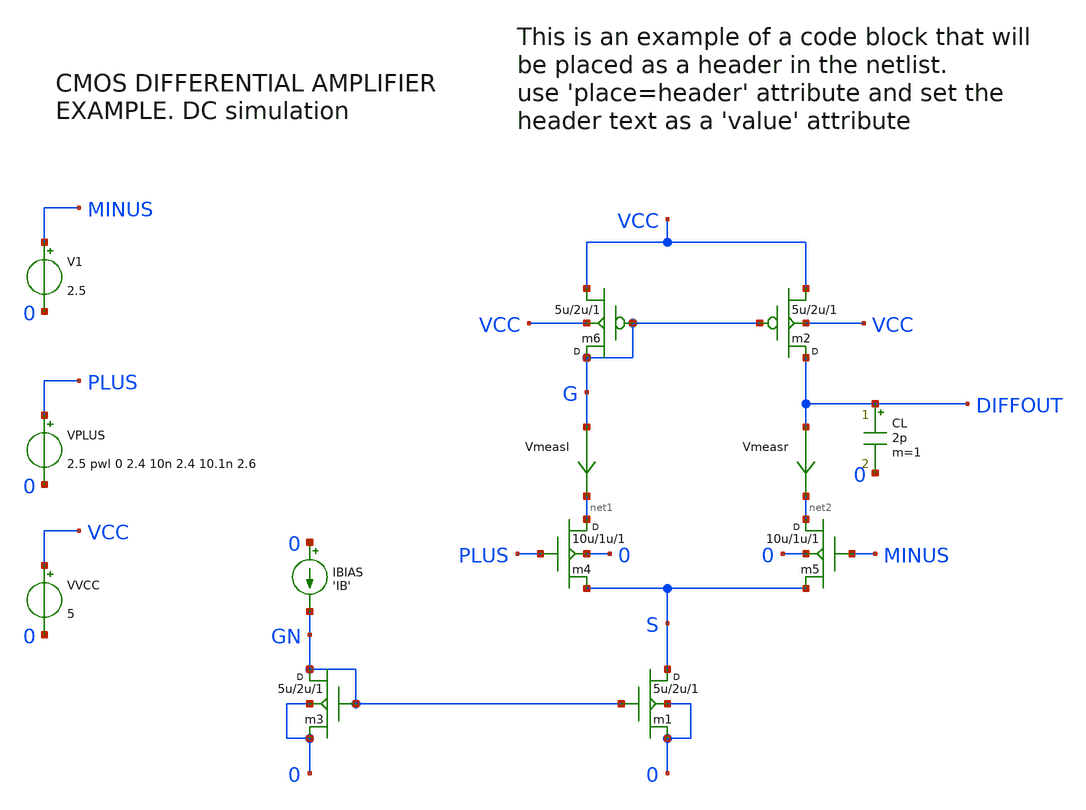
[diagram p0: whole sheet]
** sch_path: xschem_library/examples/cmos_example.sch
* Copyright (C) 1998-2023 Stefan Frederik Schippers
* This program is free software; you can redistribute it and/or modify
* it under the terms of the GNU General Public License as published by
* the Free Software Foundation; either version 2 of the License, or
* (at your option) any later version.
* This program is distributed in the hope that it will be useful,
* but WITHOUT ANY WARRANTY; without even the implied warranty of
* MERCHANTABILITY or FITNESS FOR A PARTICULAR PURPOSE.  See the
* GNU General Public License for more details.
* You should have received a copy of the GNU General Public License
* along with this program; if not, write to the Free Software

** ======================== **
** This is a netlist header **
** ======================== **

**.subckt cmos_example
m1 S GN 0 0 cmosn w=5u l=2u m=1
m2 DIFFOUT G VCC VCC cmosp w=5u l=2u m=1
VVCC VCC 0 5
m3 GN GN 0 0 cmosn w=5u l=2u m=1
IBIAS 0 GN 'IB'
m4 net1 PLUS S 0 cmosn w=10u l=1u m=1
m5 net2 MINUS S 0 cmosn w=10u l=1u m=1
m6 G G VCC VCC cmosp w=5u l=2u m=1
VPLUS PLUS 0 2.5 pwl 0 2.4 10n 2.4 10.1n 2.6
V1 MINUS 0 2.5
CL DIFFOUT 0 2p m=1
Vmeasr DIFFOUT net2 0
.save i(vmeasr)
Vmeasl G net1 0
.save i(vmeasl)
**** begin user architecture code


.temp 30
.param IB=1u
** models are generally not free: you must download
** SPICE models for active devices and put them into the below
** referenced file in netlist/simulation directory.
** http://bwrcs.eecs.berkeley.edu/Classes/icdesign/ee241_s00/ASSIGNMENTS/TSMC035-n96g-params.txt
.include "models_cmos_example.txt"
.option savecurrents
.save all @m4[gm] @m5[gm] @m1[gm]
.control
  save all
  op
  write cmos_example_ngspice.raw
  set appendwrite
  * tran 1n 300n
  dc vplus 2.3 2.7 0.001
  write cmos_example_ngspice.raw

  alterparam IB=10u
  reset
  save all
  dc vplus 2.3 2.7 0.001
  write cmos_example_ngspice.raw

  alterparam IB=100u
  reset
  save all
  dc vplus 2.3 2.7 0.001
  write cmos_example_ngspice.raw

.endc







**** end user architecture code
**.ends
.end
